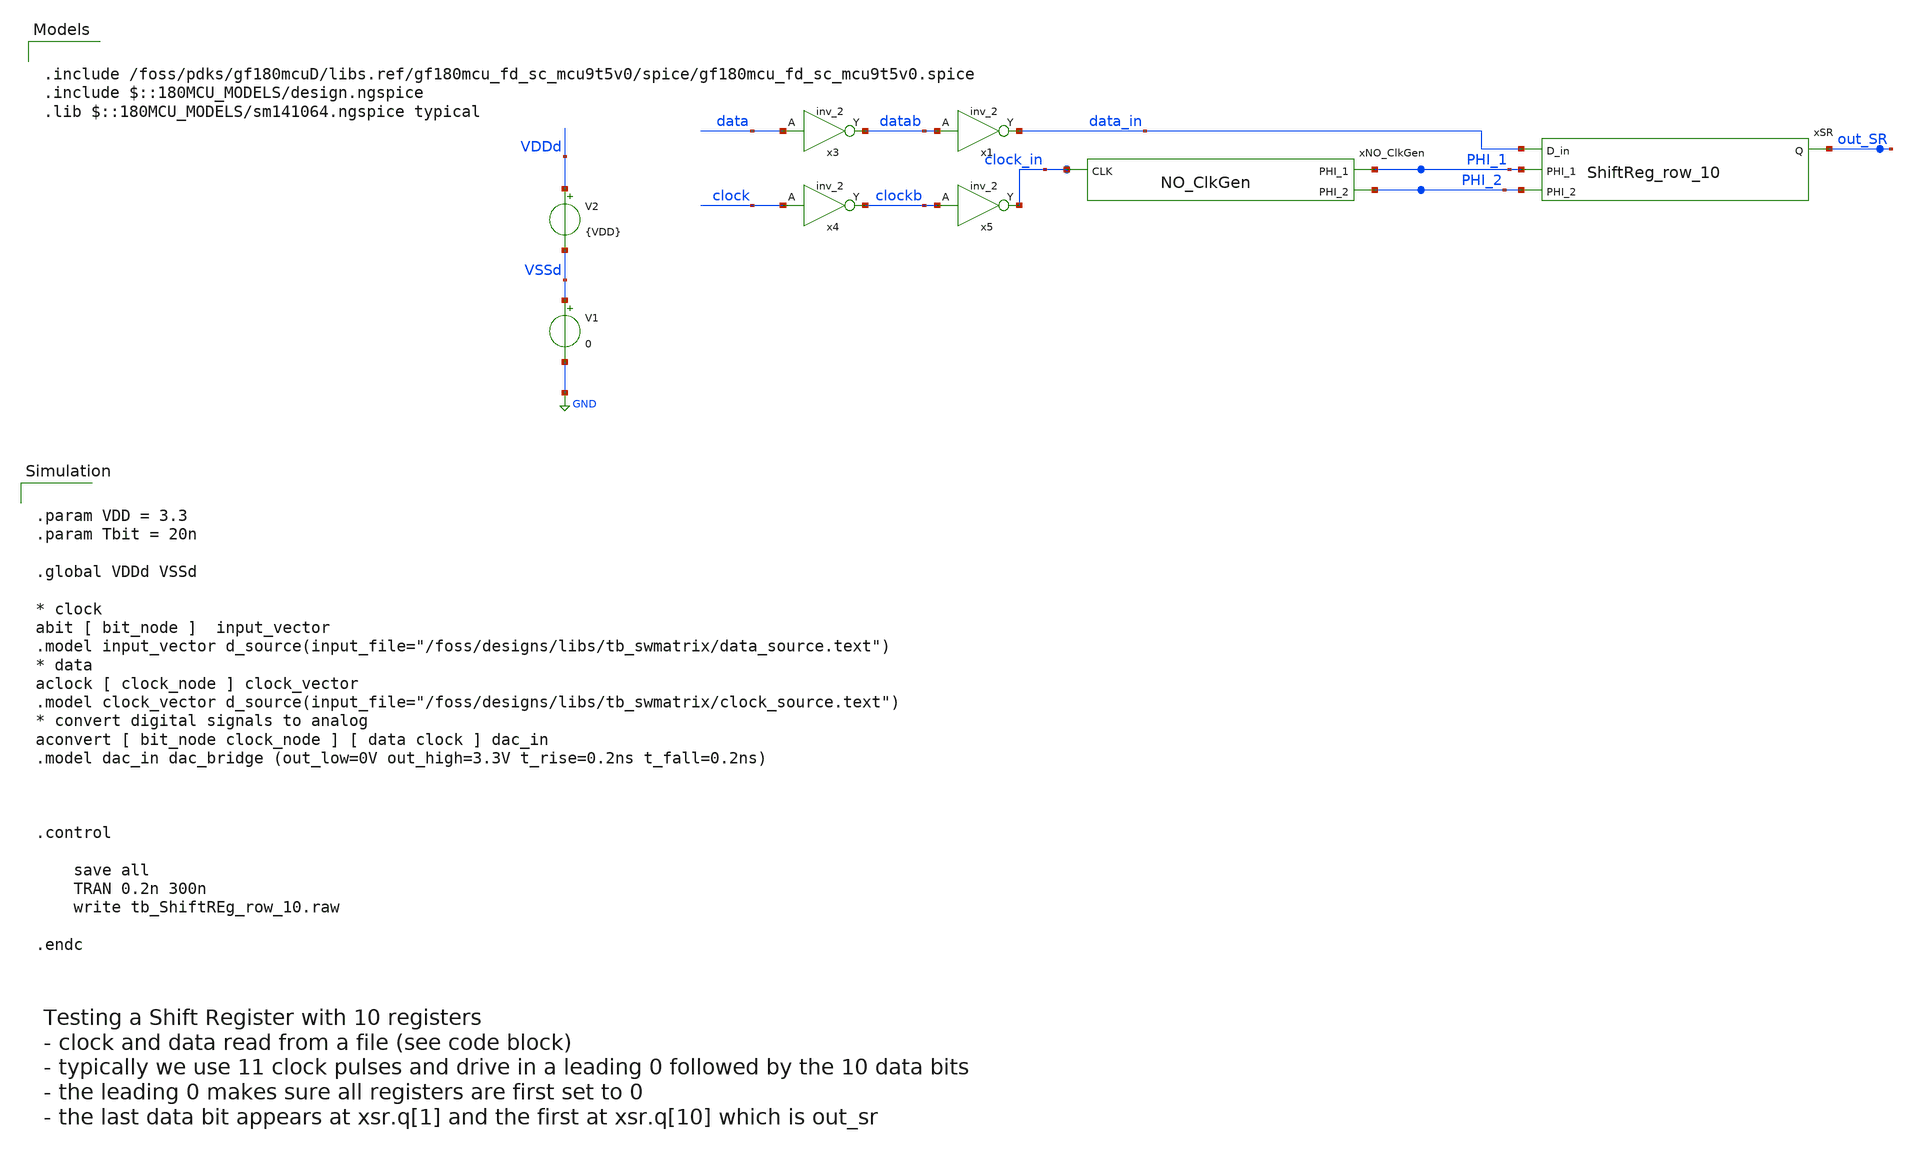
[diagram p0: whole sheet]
** sch_path: designs/switch_matrix_gf180mcu_9t5v0-main/testbenches/tb_ShiftReg_row_10.sch
**.subckt tb_ShiftReg_row_10
V1 VSSd GND 0
V2 VDDd VSSd {VDD}
xSR out_SR data_in PHI_1 PHI_2 ShiftReg_row_10
xNO_ClkGen PHI_2 clock_in PHI_1 NO_ClkGen
x3 data VSSd VDDd VSSd VDDd datab gf180mcu_fd_sc_mcu9t5v0__inv_2
x1 datab VSSd VDDd VSSd VDDd data_in gf180mcu_fd_sc_mcu9t5v0__inv_2
x4 clock VSSd VDDd VSSd VDDd clockb gf180mcu_fd_sc_mcu9t5v0__inv_2
x5 clockb VSSd VDDd VSSd VDDd clock_in gf180mcu_fd_sc_mcu9t5v0__inv_2
**** begin user architecture code


.param VDD = 3.3
.param Tbit = 20n

.global VDDd VSSd

* clock
abit [ bit_node ]  input_vector
.model input_vector d_source(input_file="/foss/designs/libs/tb_swmatrix/data_source.text")
* data
aclock [ clock_node ] clock_vector
.model clock_vector d_source(input_file="/foss/designs/libs/tb_swmatrix/clock_source.text")
* convert digital signals to analog
aconvert [ bit_node clock_node ] [ data clock ] dac_in
.model dac_in dac_bridge (out_low=0V out_high=3.3V t_rise=0.2ns t_fall=0.2ns)



.control

    save all
    TRAN 0.2n 300n
    write tb_ShiftREg_row_10.raw

.endc



.include /foss/pdks/gf180mcuD/libs.ref/gf180mcu_fd_sc_mcu9t5v0/spice/gf180mcu_fd_sc_mcu9t5v0.spice
.include $::180MCU_MODELS/design.ngspice
.lib $::180MCU_MODELS/sm141064.ngspice typical

**** end user architecture code
**.ends

* expanding   symbol:  libs/core_swmatrix/ShiftReg_row_10.sym # of pins=4
** sym_path: designs/switch_matrix_gf180mcu_9t5v0-main/designs/libs/core_swmatrix/ShiftReg_row_10.sym
** sch_path: designs/switch_matrix_gf180mcu_9t5v0-main/designs/libs/core_swmatrix/ShiftReg_row_10.sch
.subckt ShiftReg_row_10 Q D_in PHI_1 PHI_2
*.ipin PHI_1
*.ipin PHI_2
*.ipin D_in
*.opin Q
xFF[1] D_in Q[1] PHI_1 PHI_2 DFF_2phase_1
xFF[2] Q[1] Q[2] PHI_1 PHI_2 DFF_2phase_1
xFF[3] Q[2] Q[3] PHI_1 PHI_2 DFF_2phase_1
xFF[4] Q[3] Q[4] PHI_1 PHI_2 DFF_2phase_1
xFF[5] Q[4] Q[5] PHI_1 PHI_2 DFF_2phase_1
xFF[6] Q[5] Q[6] PHI_1 PHI_2 DFF_2phase_1
xFF[7] Q[6] Q[7] PHI_1 PHI_2 DFF_2phase_1
xFF[8] Q[7] Q[8] PHI_1 PHI_2 DFF_2phase_1
xFF[9] Q[8] Q[9] PHI_1 PHI_2 DFF_2phase_1
xFF[10] Q[9] Q PHI_1 PHI_2 DFF_2phase_1
.ends


* expanding   symbol:  libs/core_swmatrix/NO_ClkGen.sym # of pins=3
** sym_path: designs/switch_matrix_gf180mcu_9t5v0-main/designs/libs/core_swmatrix/NO_ClkGen.sym
** sch_path: designs/switch_matrix_gf180mcu_9t5v0-main/designs/libs/core_swmatrix/NO_ClkGen.sch
.subckt NO_ClkGen PHI_2 CLK PHI_1
*.ipin CLK
*.opin PHI_2
*.opin PHI_1
x1 CLKB OUT_bot_d VSSd VDDd VSSd VDDd OUT_top gf180mcu_fd_sc_mcu9t5v0__nand2_1
x2 OUT_top_d CLKbuf VSSd VDDd VSSd VDDd OUT_bot gf180mcu_fd_sc_mcu9t5v0__nand2_1
x3 OUT_top VSSd VDDd VSSd VDDd PHI_2 gf180mcu_fd_sc_mcu9t5v0__inv_1
x4 PHI_2 VSSd VDDd VSSd VDDd net3 gf180mcu_fd_sc_mcu9t5v0__inv_1
x5 net1 VSSd VDDd VSSd VDDd OUT_top_d gf180mcu_fd_sc_mcu9t5v0__inv_1
x6 OUT_bot VSSd VDDd VSSd VDDd PHI_1 gf180mcu_fd_sc_mcu9t5v0__inv_1
x7 PHI_1 VSSd VDDd VSSd VDDd net4 gf180mcu_fd_sc_mcu9t5v0__inv_1
x8 net2 VSSd VDDd VSSd VDDd OUT_bot_d gf180mcu_fd_sc_mcu9t5v0__inv_1
x9 CLKB VSSd VDDd VSSd VDDd CLKbuf gf180mcu_fd_sc_mcu9t5v0__inv_1
x10 CLK VSSd VDDd VSSd VDDd CLKB gf180mcu_fd_sc_mcu9t5v0__inv_1
x11 net3 VSSd VDDd VSSd VDDd net1 gf180mcu_fd_sc_mcu9t5v0__inv_1
x12 net4 VSSd VDDd VSSd VDDd net2 gf180mcu_fd_sc_mcu9t5v0__inv_1
.ends


* expanding   symbol:  libs/core_swmatrix/DFF_2phase_1.sym # of pins=4
** sym_path: designs/switch_matrix_gf180mcu_9t5v0-main/designs/libs/core_swmatrix/DFF_2phase_1.sym
** sch_path: designs/switch_matrix_gf180mcu_9t5v0-main/designs/libs/core_swmatrix/DFF_2phase_1.sch
.subckt DFF_2phase_1 D Q PHI_1 PHI_2
*.ipin D
*.ipin PHI_1
*.ipin PHI_2
*.opin Q
xmain D PHI_1 out_m VDDd VDDd VSSd VSSd gf180mcu_fd_sc_mcu9t5v0__latq_1
xsecondary out_m PHI_2 Q VDDd VDDd VSSd VSSd gf180mcu_fd_sc_mcu9t5v0__latq_1
.ends

.GLOBAL GND
.end
